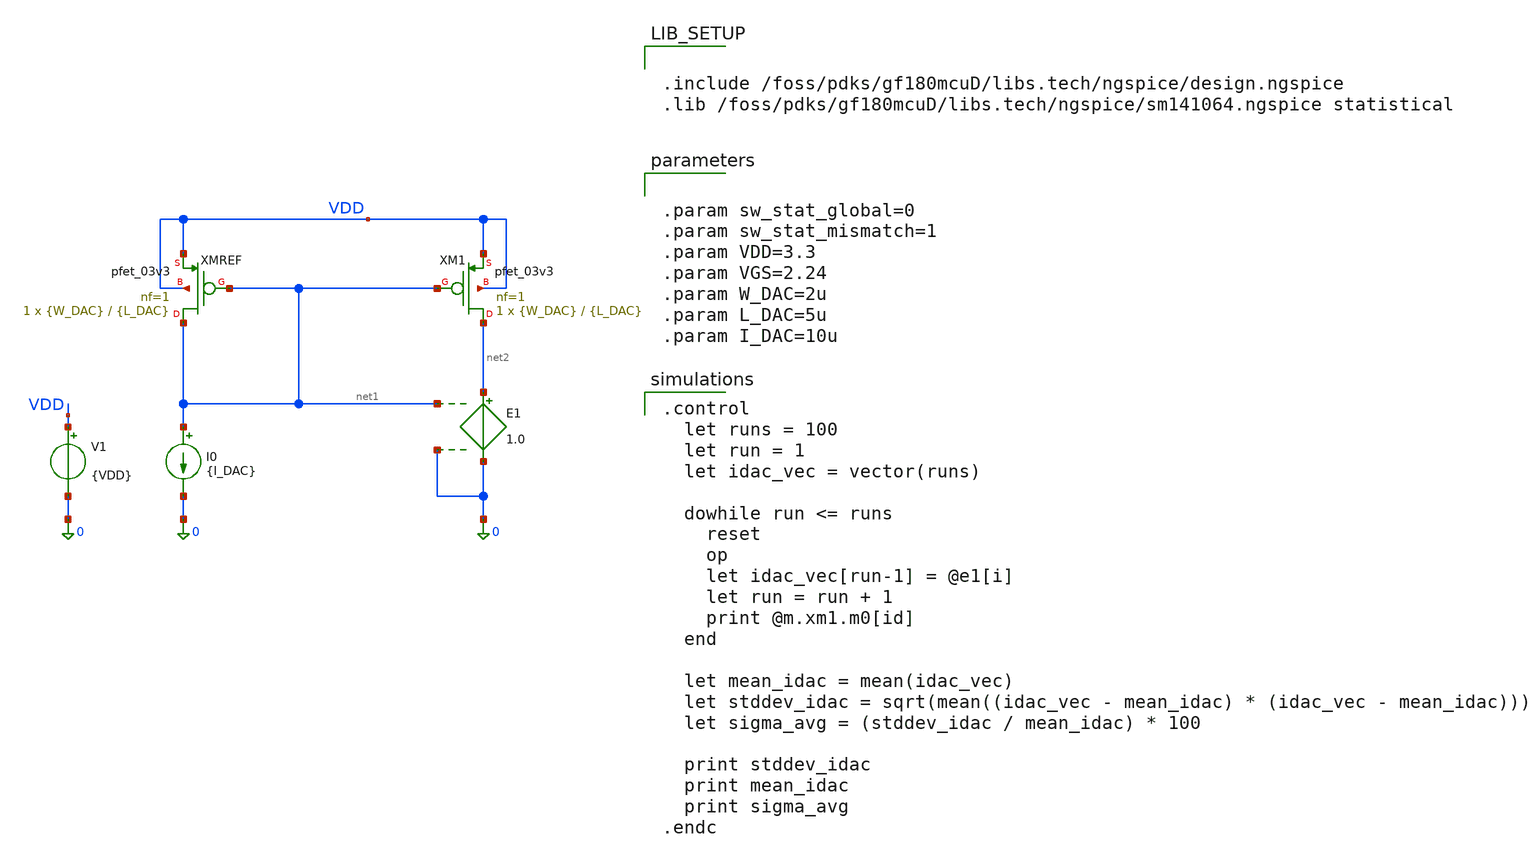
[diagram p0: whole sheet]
** sch_path: lab_2/lab2.sch
**.subckt lab2
I0 net1 0 {I_DAC}
E1 net2 0 net1 0 1.0
V1 VDD 0 {VDD}
XM1 net2 net1 VDD VDD pfet_03v3 L={L_DAC} W={W_DAC} nf=1 ad='int((nf+1)/2) * W/nf * 0.18u' as='int((nf+2)/2) * W/nf * 0.18u'
+ pd='2*int((nf+1)/2) * (W/nf + 0.18u)' ps='2*int((nf+2)/2) * (W/nf + 0.18u)' nrd='0.18u / W' nrs='0.18u / W'
+ sa=0 sb=0 sd=0 m=1
XMREF net1 net1 VDD VDD pfet_03v3 L={L_DAC} W={W_DAC} nf=1 ad='int((nf+1)/2) * W/nf * 0.18u' as='int((nf+2)/2) * W/nf * 0.18u'
+ pd='2*int((nf+1)/2) * (W/nf + 0.18u)' ps='2*int((nf+2)/2) * (W/nf + 0.18u)' nrd='0.18u / W' nrs='0.18u / W'
+ sa=0 sb=0 sd=0 m=1
**** begin user architecture code


.include /foss/pdks/gf180mcuD/libs.tech/ngspice/design.ngspice
.lib /foss/pdks/gf180mcuD/libs.tech/ngspice/sm141064.ngspice statistical




.param sw_stat_global=0
.param sw_stat_mismatch=1
.param VDD=3.3
.param VGS=2.24
.param W_DAC=2u
.param L_DAC=5u
.param I_DAC=10u



.control
  let runs = 100
  let run = 1
  let idac_vec = vector(runs)

  dowhile run <= runs
    reset
    op
    let idac_vec[run-1] = @e1[i]
    let run = run + 1
    print @m.xm1.m0[id]
  end

  let mean_idac = mean(idac_vec)
  let stddev_idac = sqrt(mean((idac_vec - mean_idac) * (idac_vec - mean_idac)))
  let sigma_avg = (stddev_idac / mean_idac) * 100

  print stddev_idac
  print mean_idac
  print sigma_avg
.endc


**** end user architecture code
**.ends
.end
